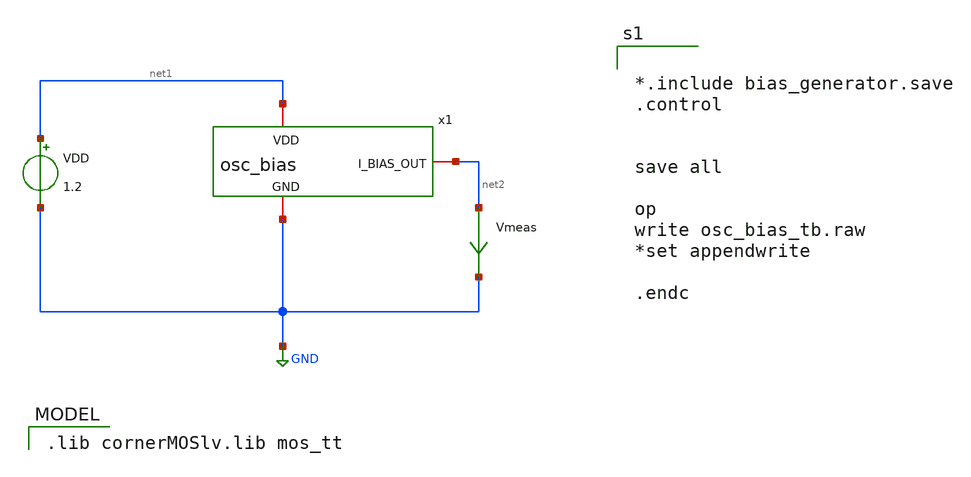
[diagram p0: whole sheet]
** sch_path: osc_bias_tb.sch
**.subckt osc_bias_tb
VDD net1 GND 1.2
Vmeas net2 GND 0
.save i(vmeas)
x1 net1 net2 GND osc_bias
**** begin user architecture code
 .lib cornerMOSlv.lib mos_tt



*.include bias_generator.save
.control


save all

op
write osc_bias_tb.raw
*set appendwrite

.endc


**** end user architecture code
**.ends

* expanding   symbol:  /foss/designs/xtal/osc_bias.sym # of pins=3
** sym_path: osc_bias.sym
** sch_path: osc_bias.sch
.subckt osc_bias VDD I_BIAS_OUT GND
*.iopin VDD
*.iopin GND
*.iopin I_BIAS_OUT
XM1 vp_bias vp_bias VDD VDD sg13_lv_pmos w=0.5u l=10u ng=1 m=1 mm_ok=1
XM3 vp_bias vp_bias net2 net1 sg13_lv_nmos w=0.25u l=15u ng=1 m=1 mm_ok=1
XM4 net2 net2 net3 net1 sg13_lv_nmos w=0.25u l=15u ng=1 m=1 mm_ok=1
XM5 net3 net3 net1 net1 sg13_lv_nmos w=0.25u l=15u ng=1 m=1 mm_ok=1
XM2 I_BIAS_OUT vp_bias VDD VDD sg13_lv_pmos w=0.5u l=10u ng=1 m=1 mm_ok=1
Vmeas_ref_path net1 GND 0
.save i(vmeas_ref_path)
.ends

.GLOBAL GND
.end
